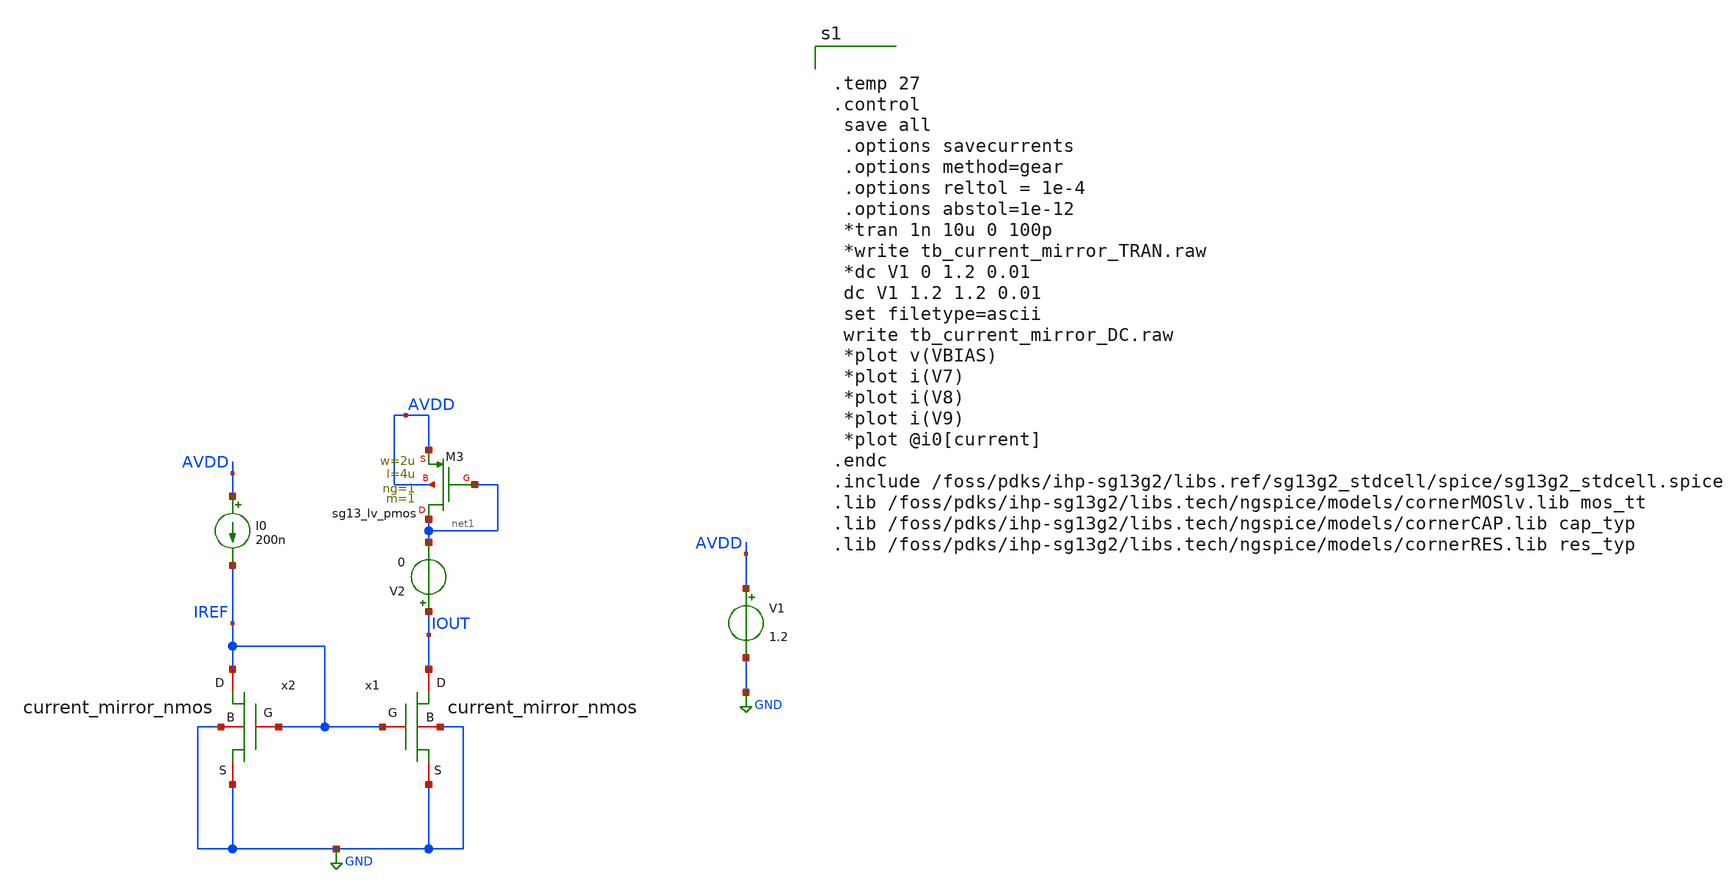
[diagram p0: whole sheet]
** sch_path: DAC/tb_current_mirror.sch
**.subckt tb_current_mirror
I0 AVDD IREF 200n
V1 AVDD GND 1.2
XM3 net1 net1 AVDD AVDD sg13_lv_pmos w=2u l=4u ng=1 m=1 mm_ok=1
V2 IOUT net1 0
x1 IOUT GND IREF GND current_mirror_nmos
x2 IREF GND IREF GND current_mirror_nmos
**** begin user architecture code


.temp 27
.control
 save all
 .options savecurrents
 .options method=gear
 .options reltol = 1e-4
 .options abstol=1e-12
 *tran 1n 10u 0 100p
 *write tb_current_mirror_TRAN.raw
 *dc V1 0 1.2 0.01
 dc V1 1.2 1.2 0.01
 set filetype=ascii
 write tb_current_mirror_DC.raw
 *plot v(VBIAS)
 *plot i(V7)
 *plot i(V8)
 *plot i(V9)
 *plot @i0[current]
.endc
.include /foss/pdks/ihp-sg13g2/libs.ref/sg13g2_stdcell/spice/sg13g2_stdcell.spice
.lib /foss/pdks/ihp-sg13g2/libs.tech/ngspice/models/cornerMOSlv.lib mos_tt
.lib /foss/pdks/ihp-sg13g2/libs.tech/ngspice/models/cornerCAP.lib cap_typ
.lib /foss/pdks/ihp-sg13g2/libs.tech/ngspice/models/cornerRES.lib res_typ


**** end user architecture code
**.ends
.GLOBAL GND
.end
